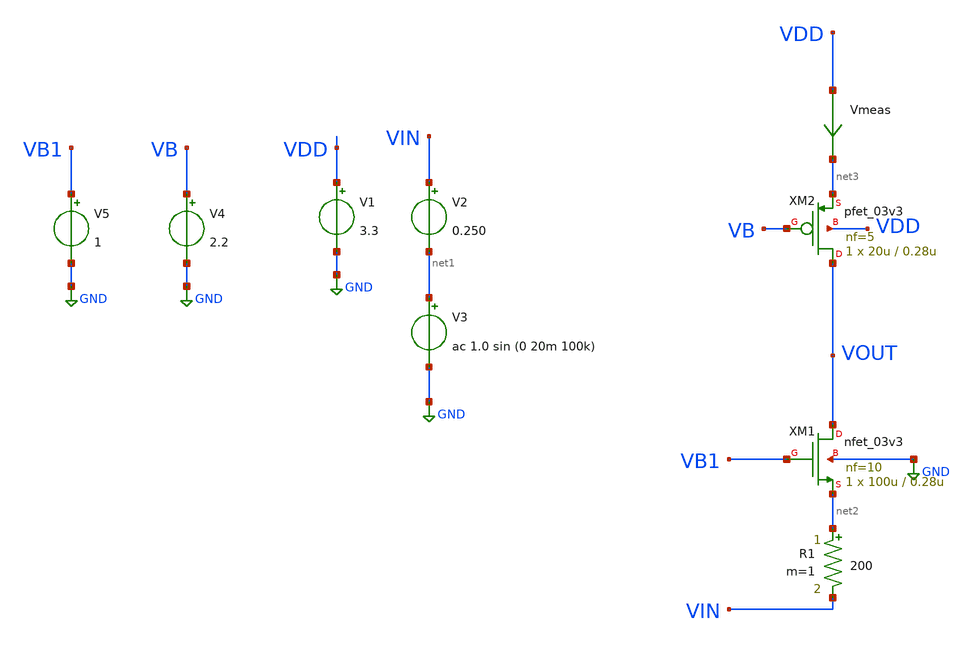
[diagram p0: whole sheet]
** sch_path: simple_amp10.sch
**.subckt simple_amp10
XM1 VOUT VB1 net2 GND nfet_03v3 L=0.28u W=100u nf=10 ad='int((nf+1)/2) * W/nf * 0.18u' as='int((nf+2)/2) * W/nf * 0.18u'
+ pd='2*int((nf+1)/2) * (W/nf + 0.18u)' ps='2*int((nf+2)/2) * (W/nf + 0.18u)' nrd='0.18u / W' nrs='0.18u / W'
+ sa=0 sb=0 sd=0 m=1
Vmeas VDD net3 0
.save i(vmeas)
V1 VDD GND 3.3
V2 VIN net1 0.250
V3 net1 GND ac 1.0 sin (0 20m 100k)
XM2 VOUT VB net3 VDD pfet_03v3 L=0.28u W=20u nf=5 ad='int((nf+1)/2) * W/nf * 0.18u' as='int((nf+2)/2) * W/nf * 0.18u'
+ pd='2*int((nf+1)/2) * (W/nf + 0.18u)' ps='2*int((nf+2)/2) * (W/nf + 0.18u)' nrd='0.18u / W' nrs='0.18u / W'
+ sa=0 sb=0 sd=0 m=1
V4 VB GND 2.2
R1 net2 VIN 200 m=1
V5 VB1 GND 1
**** begin user architecture code

.include $::180MCU_MODELS/design.ngspice
*.lib $::180MCU_MODELS/sm141064.ngspice statistical
*.lib $::180MCU_MODELS/sm141064.ngspice res_statistical
.lib $::180MCU_MODELS/sm141064.ngspice typical
.lib $::180MCU_MODELS/sm141064.ngspice res_typical
.lib $::180MCU_MODELS/sm141064.ngspice moscap_typical
.lib $::180MCU_MODELS/sm141064.ngspice bjt_typical
.lib $::180MCU_MODELS/sm141064.ngspice diode_typical
.lib $::180MCU_MODELS/sm141064.ngspice mimcap_typical
.TEMP 27

.param   sw_stat_global = 1   sw_stat_mism = 1  mc_skew = 3  res_mc_skew = 3  cap_mc_skew = 3
+  fnoicor = 1



.control
save all
dc V2 0 3.3 0.01


plot v(VOUT) deriv(v(VOUT)) v(VIN)
plot deriv(v(VOUT)) (v(VDD)-v(VG)) (v(VDD)-v(VOUT))
plot i(Vmeas)
plot deriv(v(VOUT))
tran 10ns 20u
plot (v(VOUT)-1.8318) (v(VIN)-0.250)
plot fft((v(VOUT))) fft((v(VIN)))
ac dec 20 1 50G
plot v(VOUT)
.endc

**** end user architecture code
**.ends
.GLOBAL GND
.end
